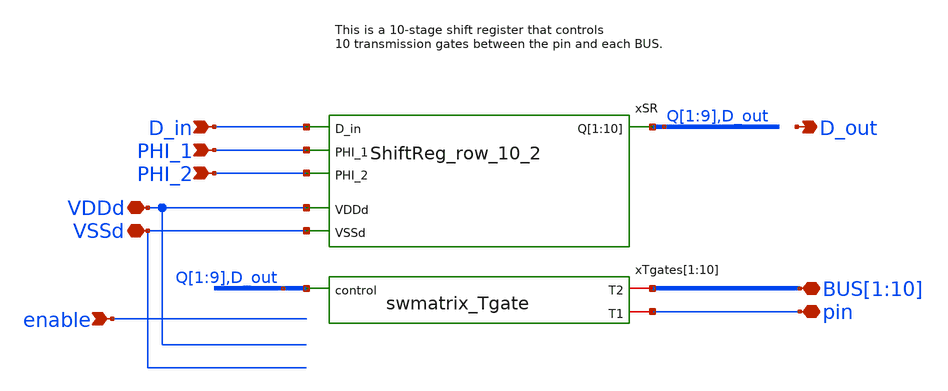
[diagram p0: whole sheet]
** sch_path: designs/switch_matrix_gf180mcu_9t5v0-main/swmatrix_row_10/swmatrix_row_10.sch
**.subckt swmatrix_row_10 pin PHI_2 PHI_1
*+ BUS[1],BUS[2],BUS[3],BUS[4],BUS[5],BUS[6],BUS[7],BUS[8],BUS[9],BUS[10] D_in D_out VDDd VSSd enable
*.iopin pin
*.ipin PHI_2
*.ipin PHI_1
*.iopin BUS[1],BUS[2],BUS[3],BUS[4],BUS[5],BUS[6],BUS[7],BUS[8],BUS[9],BUS[10]
*.ipin D_in
*.opin D_out
*.iopin VDDd
*.iopin VSSd
*.ipin enable
xSR Q[1] Q[2] Q[3] Q[4] Q[5] Q[6] Q[7] Q[8] Q[9] D_out D_in PHI_1 PHI_2 VDDd VSSd ShiftReg_row_10_2
xTgates[1] Q[1] BUS[1] pin swmatrix_Tgate
xTgates[2] Q[2] BUS[2] pin swmatrix_Tgate
xTgates[3] Q[3] BUS[3] pin swmatrix_Tgate
xTgates[4] Q[4] BUS[4] pin swmatrix_Tgate
xTgates[5] Q[5] BUS[5] pin swmatrix_Tgate
xTgates[6] Q[6] BUS[6] pin swmatrix_Tgate
xTgates[7] Q[7] BUS[7] pin swmatrix_Tgate
xTgates[8] Q[8] BUS[8] pin swmatrix_Tgate
xTgates[9] Q[9] BUS[9] pin swmatrix_Tgate
xTgates[10] D_out BUS[10] pin swmatrix_Tgate
**.ends

* expanding   symbol:  switch_matrix_gf180mcu_9t5v0/ShiftReg_row_10_2/ShiftReg_row_10_2.sym # of
*+ pins=6
** sym_path: designs/switch_matrix_gf180mcu_9t5v0-main/ShiftReg_row_10_2/ShiftReg_row_10_2.sym
** sch_path: designs/switch_matrix_gf180mcu_9t5v0-main/ShiftReg_row_10_2/ShiftReg_row_10_2.sch
.subckt ShiftReg_row_10_2 Q[1] Q[2] Q[3] Q[4] Q[5] Q[6] Q[7] Q[8] Q[9] Q[10] D_in PHI_1 PHI_2 VDDd
+ VSSd
*.ipin PHI_1
*.ipin PHI_2
*.ipin D_in
*.opin Q[1],Q[2],Q[3],Q[4],Q[5],Q[6],Q[7],Q[8],Q[9],Q[10]
*.iopin VDDd
*.iopin VSSd
xFF[1] D_in Q[1] PHI_1 PHI_2 DFF_2phase_1
xFF[2] Q[1] Q[2] PHI_1 PHI_2 DFF_2phase_1
xFF[3] Q[2] Q[3] PHI_1 PHI_2 DFF_2phase_1
xFF[4] Q[3] Q[4] PHI_1 PHI_2 DFF_2phase_1
xFF[5] Q[4] Q[5] PHI_1 PHI_2 DFF_2phase_1
xFF[6] Q[5] Q[6] PHI_1 PHI_2 DFF_2phase_1
xFF[7] Q[6] Q[7] PHI_1 PHI_2 DFF_2phase_1
xFF[8] Q[7] Q[8] PHI_1 PHI_2 DFF_2phase_1
xFF[9] Q[8] Q[9] PHI_1 PHI_2 DFF_2phase_1
xFF[10] Q[9] Q[10] PHI_1 PHI_2 DFF_2phase_1
.ends


* expanding   symbol:  switch_matrix_gf180mcu_9t5v0/swmatrix_Tgate/swmatrix_Tgate.sym # of pins=3
** sym_path: designs/switch_matrix_gf180mcu_9t5v0-main/designs/libs/core_swmatrix/swmatrix_Tgate.sym
** sch_path: designs/switch_matrix_gf180mcu_9t5v0-main/designs/libs/core_swmatrix/swmatrix_Tgate.sch
.subckt swmatrix_Tgate control T2 T1
*.iopin T1
*.iopin T2
*.ipin control
* noconn control
* noconn T1
* noconn T2
.ends


* expanding   symbol:  switch_matrix_gf180mcu_9t5v0/DFF_2phase_1/DFF_2phase_1.sym # of pins=4
** sym_path: designs/switch_matrix_gf180mcu_9t5v0-main/designs/libs/core_swmatrix/DFF_2phase_1.sym
** sch_path: designs/switch_matrix_gf180mcu_9t5v0-main/designs/libs/core_swmatrix/DFF_2phase_1.sch
.subckt DFF_2phase_1 D Q PHI_1 PHI_2
*.ipin D
*.ipin PHI_1
*.ipin PHI_2
*.opin Q
xmain D PHI_1 out_m VDDd VDDd VSSd VSSd gf180mcu_fd_sc_mcu9t5v0__latq_1
xsecondary out_m PHI_2 Q VDDd VDDd VSSd VSSd gf180mcu_fd_sc_mcu9t5v0__latq_1
.ends

.end
